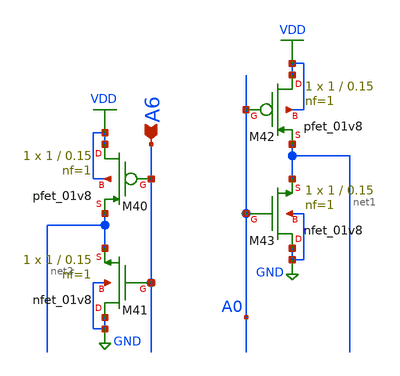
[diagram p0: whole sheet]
** sch_path: circuits/scripts/schematics/decoder_out_2_rows_head.sch
**.subckt decoder_out_2_rows_head A6
*.ipin A6
XM40 VDD A6 net2 VDD sky130_fd_pr__pfet_01v8 L=0.15 W=1 nf=1 ad='int((nf+1)/2) * W/nf * 0.29' as='int((nf+2)/2) * W/nf * 0.29'
+ pd='2*int((nf+1)/2) * (W/nf + 0.29)' ps='2*int((nf+2)/2) * (W/nf + 0.29)' nrd='0.29 / W' nrs='0.29 / W'
+ sa=0 sb=0 sd=0 mult=1 m=1
XM41 GND A6 net2 GND sky130_fd_pr__nfet_01v8 L=0.15 W=1 nf=1 ad='int((nf+1)/2) * W/nf * 0.29' as='int((nf+2)/2) * W/nf * 0.29'
+ pd='2*int((nf+1)/2) * (W/nf + 0.29)' ps='2*int((nf+2)/2) * (W/nf + 0.29)' nrd='0.29 / W' nrs='0.29 / W'
+ sa=0 sb=0 sd=0 mult=1 m=1
XM42 VDD A0 net1 VDD sky130_fd_pr__pfet_01v8 L=0.15 W=1 nf=1 ad='int((nf+1)/2) * W/nf * 0.29' as='int((nf+2)/2) * W/nf * 0.29'
+ pd='2*int((nf+1)/2) * (W/nf + 0.29)' ps='2*int((nf+2)/2) * (W/nf + 0.29)' nrd='0.29 / W' nrs='0.29 / W'
+ sa=0 sb=0 sd=0 mult=1 m=1
XM43 GND A0 net1 GND sky130_fd_pr__nfet_01v8 L=0.15 W=1 nf=1 ad='int((nf+1)/2) * W/nf * 0.29' as='int((nf+2)/2) * W/nf * 0.29'
+ pd='2*int((nf+1)/2) * (W/nf + 0.29)' ps='2*int((nf+2)/2) * (W/nf + 0.29)' nrd='0.29 / W' nrs='0.29 / W'
+ sa=0 sb=0 sd=0 mult=1 m=1
**.ends
.GLOBAL VDD
.GLOBAL GND
.end
